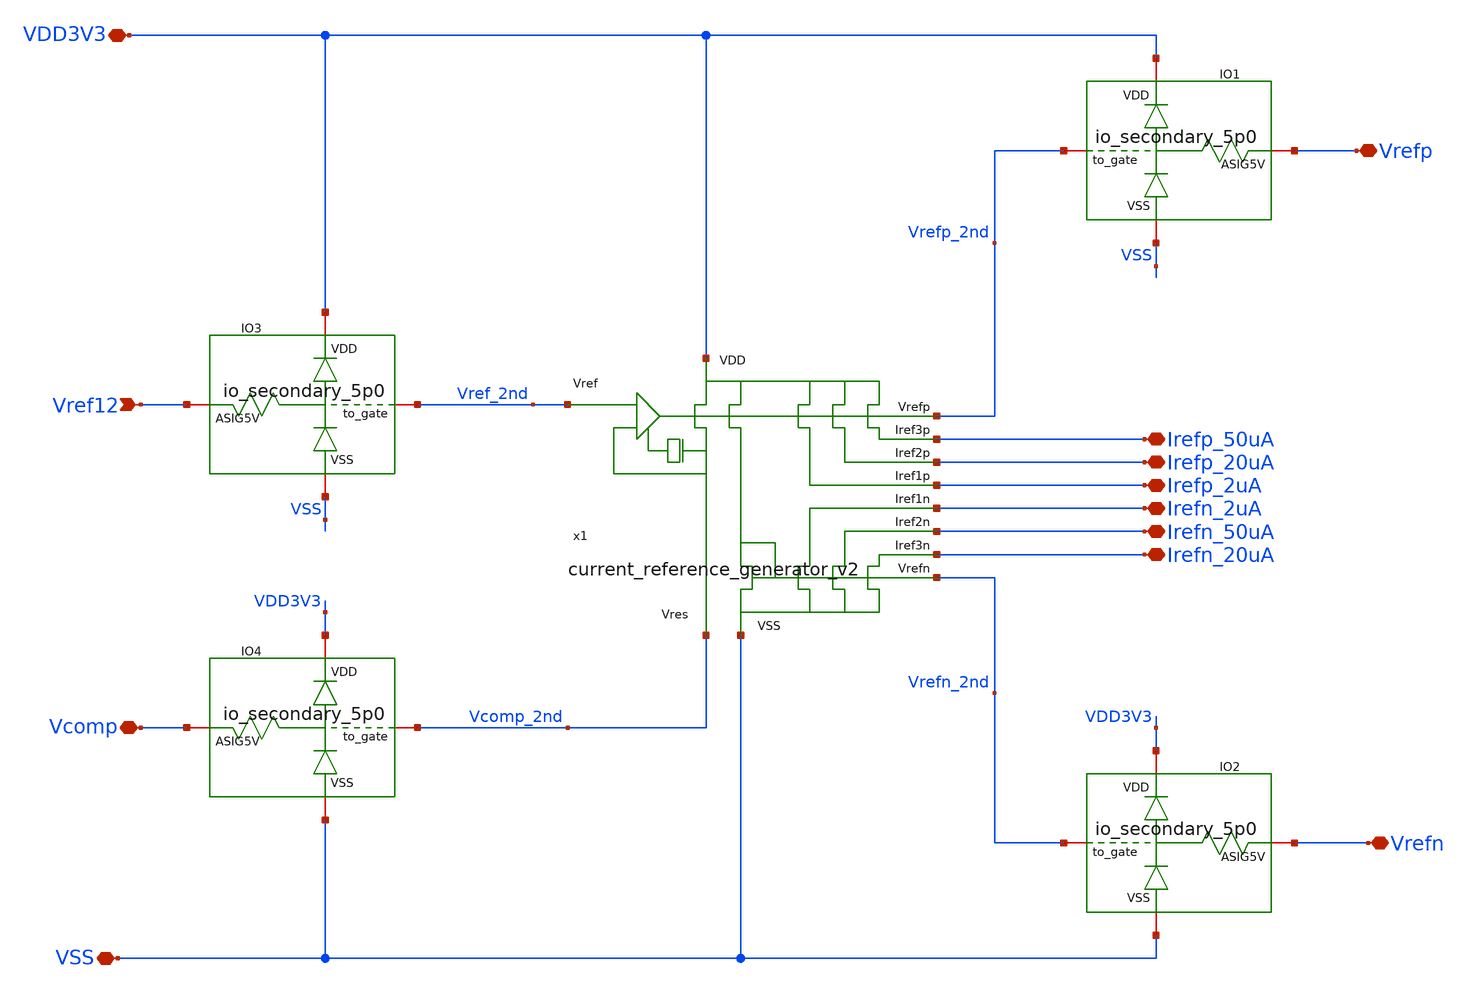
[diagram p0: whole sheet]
** sch_path: designs/libs/Axx_core/Axx_top/Axx_Current_Reference_Chip.sch
**.subckt Axx_Current_Reference_Chip Vref12 VDD3V3 VSS Vrefp Vrefn Irefn_50uA Irefn_2uA Irefp_2uA
*+ Irefp_50uA Irefn_20uA Irefp_20uA Vcomp
*.ipin Vref12
*.iopin VDD3V3
*.iopin VSS
*.iopin Vrefp
*.iopin Vrefn
*.iopin Irefn_50uA
*.iopin Irefn_2uA
*.iopin Irefp_2uA
*.iopin Irefp_50uA
*.iopin Irefn_20uA
*.iopin Irefp_20uA
*.iopin Vcomp
x1 VSS VDD3V3 Vref_2nd Vrefp_2nd Vrefn_2nd Irefn_2uA Irefn_20uA Irefp_2uA Irefp_50uA Vcomp_2nd
+ Irefn_50uA Irefp_20uA current_reference_generator_v2
XIO1 VDD3V3 Vrefp_2nd Vrefp VSS io_secondary_5p0
XIO2 VDD3V3 Vrefn_2nd Vrefn VSS io_secondary_5p0
XIO3 VDD3V3 Vref_2nd Vref12 VSS io_secondary_5p0
XIO4 VDD3V3 Vcomp_2nd Vcomp VSS io_secondary_5p0
**.ends
.end
